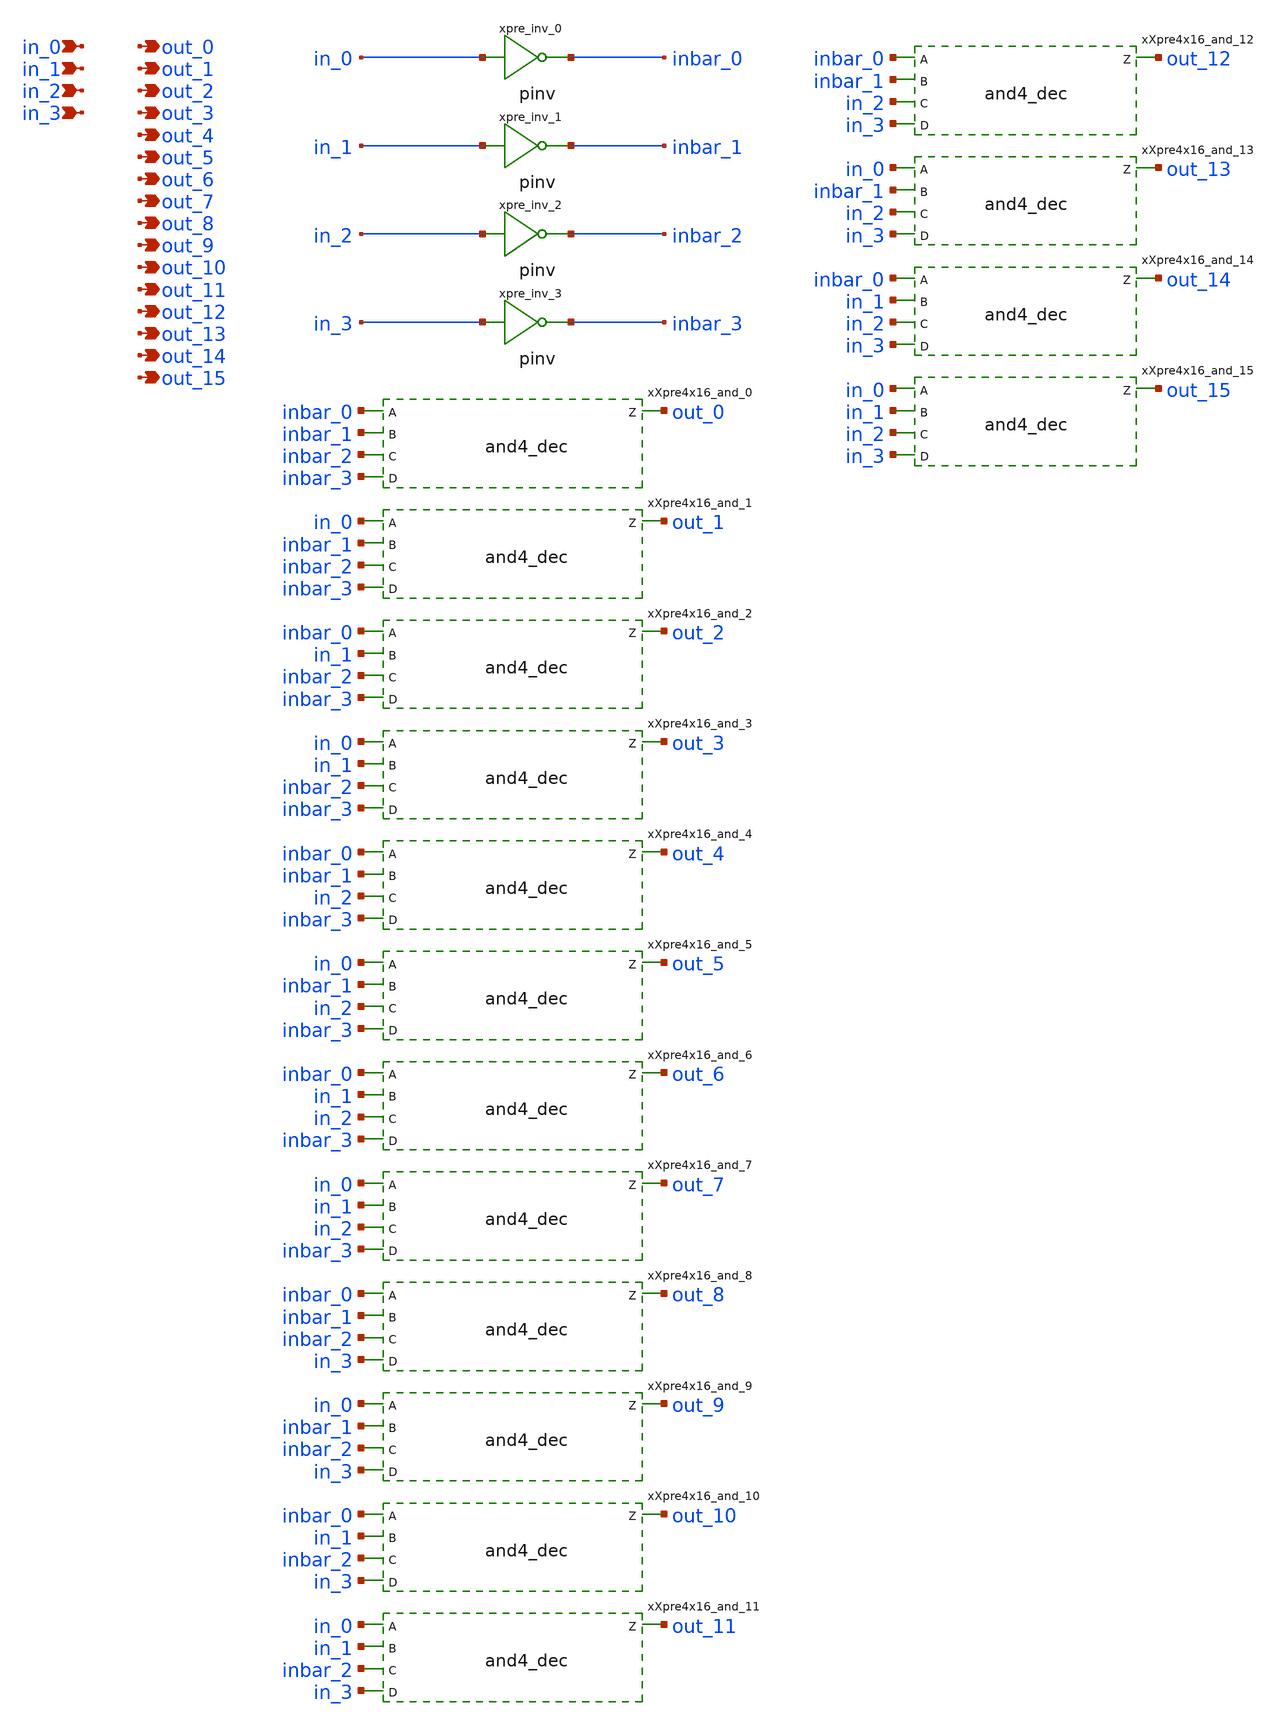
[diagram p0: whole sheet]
** sch_path: sram_2_64_scn4m_lcc/hierarchical_predecode4x16.sch
**.subckt hierarchical_predecode4x16 in_0 in_1 in_2 in_3 out_0 out_1 out_2 out_3 out_4 out_5 out_6
*+ out_7 out_8 out_9 out_10 out_11 out_12 out_13 out_14 out_15
*.ipin in_0
*.ipin in_1
*.ipin in_2
*.ipin in_3
*.opin out_0
*.opin out_1
*.opin out_2
*.opin out_3
*.opin out_4
*.opin out_5
*.opin out_6
*.opin out_7
*.opin out_8
*.opin out_9
*.opin out_10
*.opin out_11
*.opin out_12
*.opin out_13
*.opin out_14
*.opin out_15
xpre_inv_0 in_0 inbar_0 vdd gnd pinv
xpre_inv_1 in_1 inbar_1 vdd gnd pinv
xpre_inv_2 in_2 inbar_2 vdd gnd pinv
xpre_inv_3 in_3 inbar_3 vdd gnd pinv
xXpre4x16_and_0 inbar_0 inbar_1 inbar_2 inbar_3 out_0 vdd gnd and4_dec
xXpre4x16_and_1 in_0 inbar_1 inbar_2 inbar_3 out_1 vdd gnd and4_dec
xXpre4x16_and_2 inbar_0 in_1 inbar_2 inbar_3 out_2 vdd gnd and4_dec
xXpre4x16_and_3 in_0 in_1 inbar_2 inbar_3 out_3 vdd gnd and4_dec
xXpre4x16_and_4 inbar_0 inbar_1 in_2 inbar_3 out_4 vdd gnd and4_dec
xXpre4x16_and_5 in_0 inbar_1 in_2 inbar_3 out_5 vdd gnd and4_dec
xXpre4x16_and_6 inbar_0 in_1 in_2 inbar_3 out_6 vdd gnd and4_dec
xXpre4x16_and_7 in_0 in_1 in_2 inbar_3 out_7 vdd gnd and4_dec
xXpre4x16_and_8 inbar_0 inbar_1 inbar_2 in_3 out_8 vdd gnd and4_dec
xXpre4x16_and_9 in_0 inbar_1 inbar_2 in_3 out_9 vdd gnd and4_dec
xXpre4x16_and_10 inbar_0 in_1 inbar_2 in_3 out_10 vdd gnd and4_dec
xXpre4x16_and_11 in_0 in_1 inbar_2 in_3 out_11 vdd gnd and4_dec
xXpre4x16_and_12 inbar_0 inbar_1 in_2 in_3 out_12 vdd gnd and4_dec
xXpre4x16_and_13 in_0 inbar_1 in_2 in_3 out_13 vdd gnd and4_dec
xXpre4x16_and_14 inbar_0 in_1 in_2 in_3 out_14 vdd gnd and4_dec
xXpre4x16_and_15 in_0 in_1 in_2 in_3 out_15 vdd gnd and4_dec
**.ends
.end
